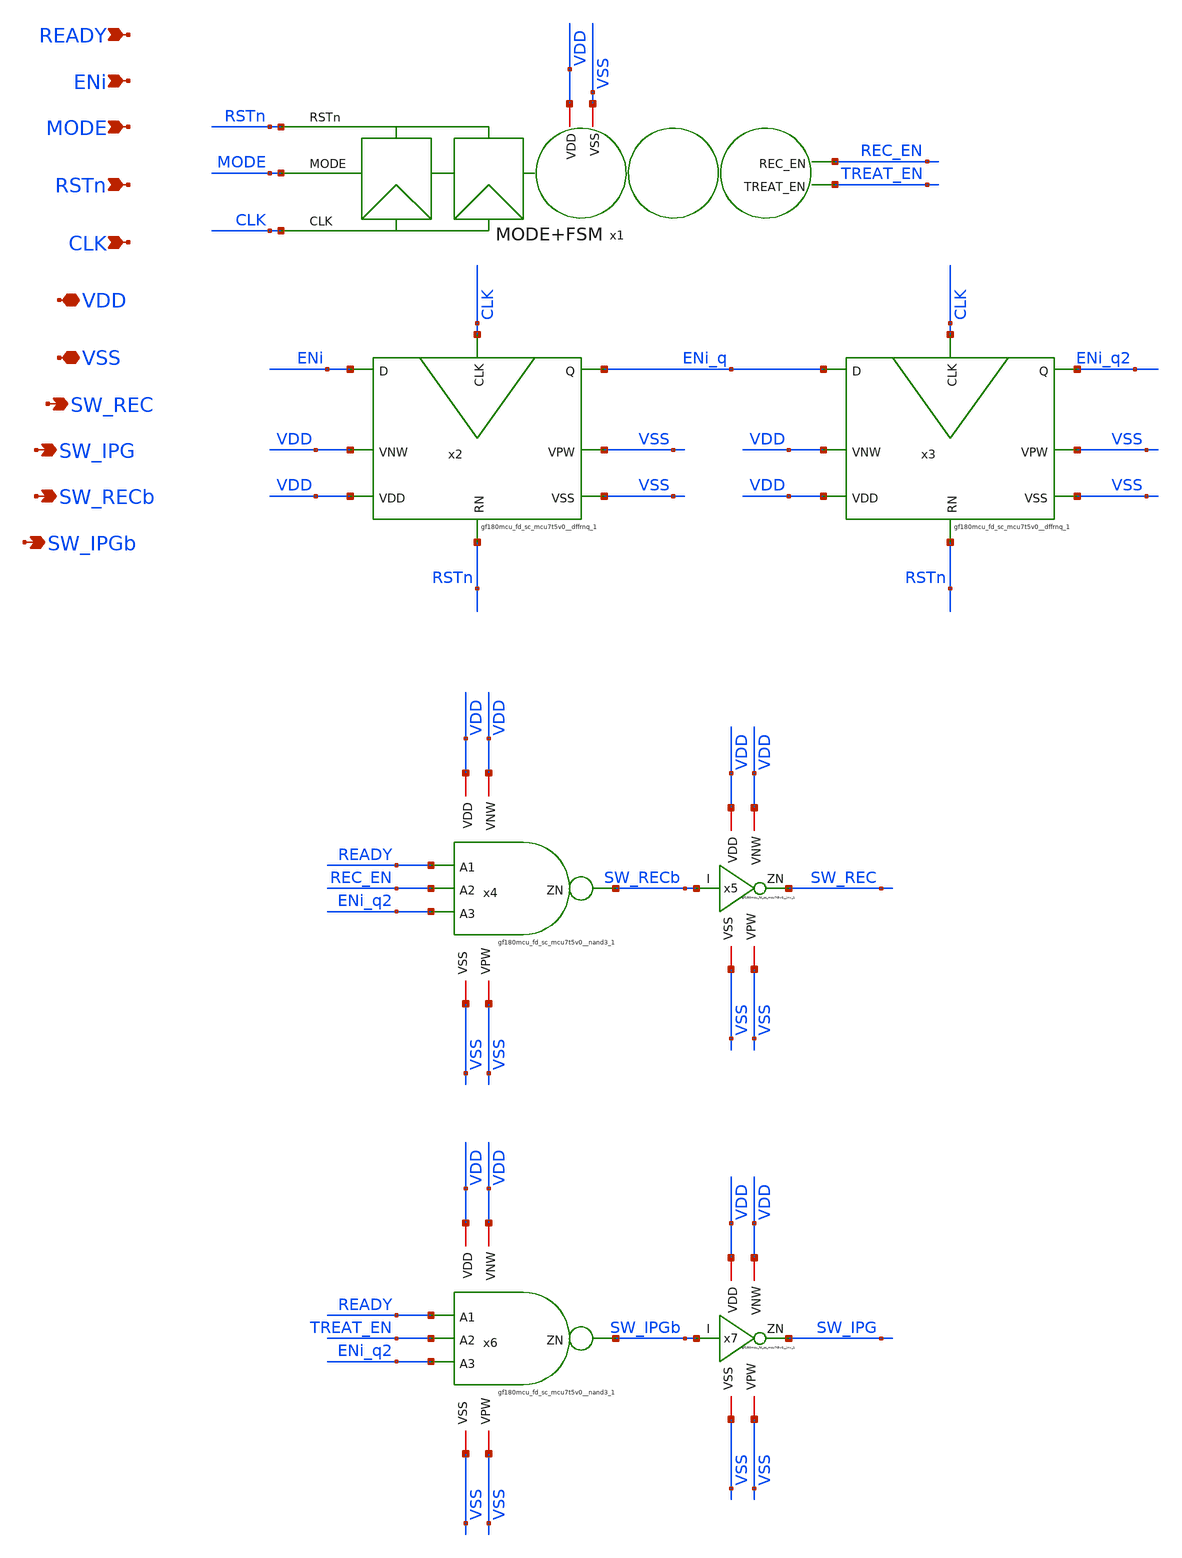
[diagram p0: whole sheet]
** sch_path: RDY/READY_sweep/CHANNEL.sch
**.subckt CHANNEL MODE RSTn CLK VDD VSS SW_REC SW_IPG SW_RECb SW_IPGb ENi READY
*.ipin MODE
*.ipin RSTn
*.ipin CLK
*.iopin VDD
*.iopin VSS
*.opin SW_REC
*.opin SW_IPG
*.opin SW_RECb
*.opin SW_IPGb
*.ipin ENi
*.ipin READY
x1 MODE RSTn CLK VDD VSS REC_EN TREAT_EN MODE+FSM
x2 ENi RSTn CLK ENi_q VDD VDD VSS VSS gf180mcu_fd_sc_mcu7t5v0__dffrnq_1
x3 ENi_q RSTn CLK ENi_q2 VDD VDD VSS VSS gf180mcu_fd_sc_mcu7t5v0__dffrnq_1
x4 READY REC_EN ENi_q2 SW_RECb VDD VDD VSS VSS gf180mcu_fd_sc_mcu7t5v0__nand3_1
x5 SW_RECb SW_REC VDD VDD VSS VSS gf180mcu_fd_sc_mcu7t5v0__inv_1
x6 READY TREAT_EN ENi_q2 SW_IPGb VDD VDD VSS VSS gf180mcu_fd_sc_mcu7t5v0__nand3_1
x7 SW_IPGb SW_IPG VDD VDD VSS VSS gf180mcu_fd_sc_mcu7t5v0__inv_1
**.ends
.end
